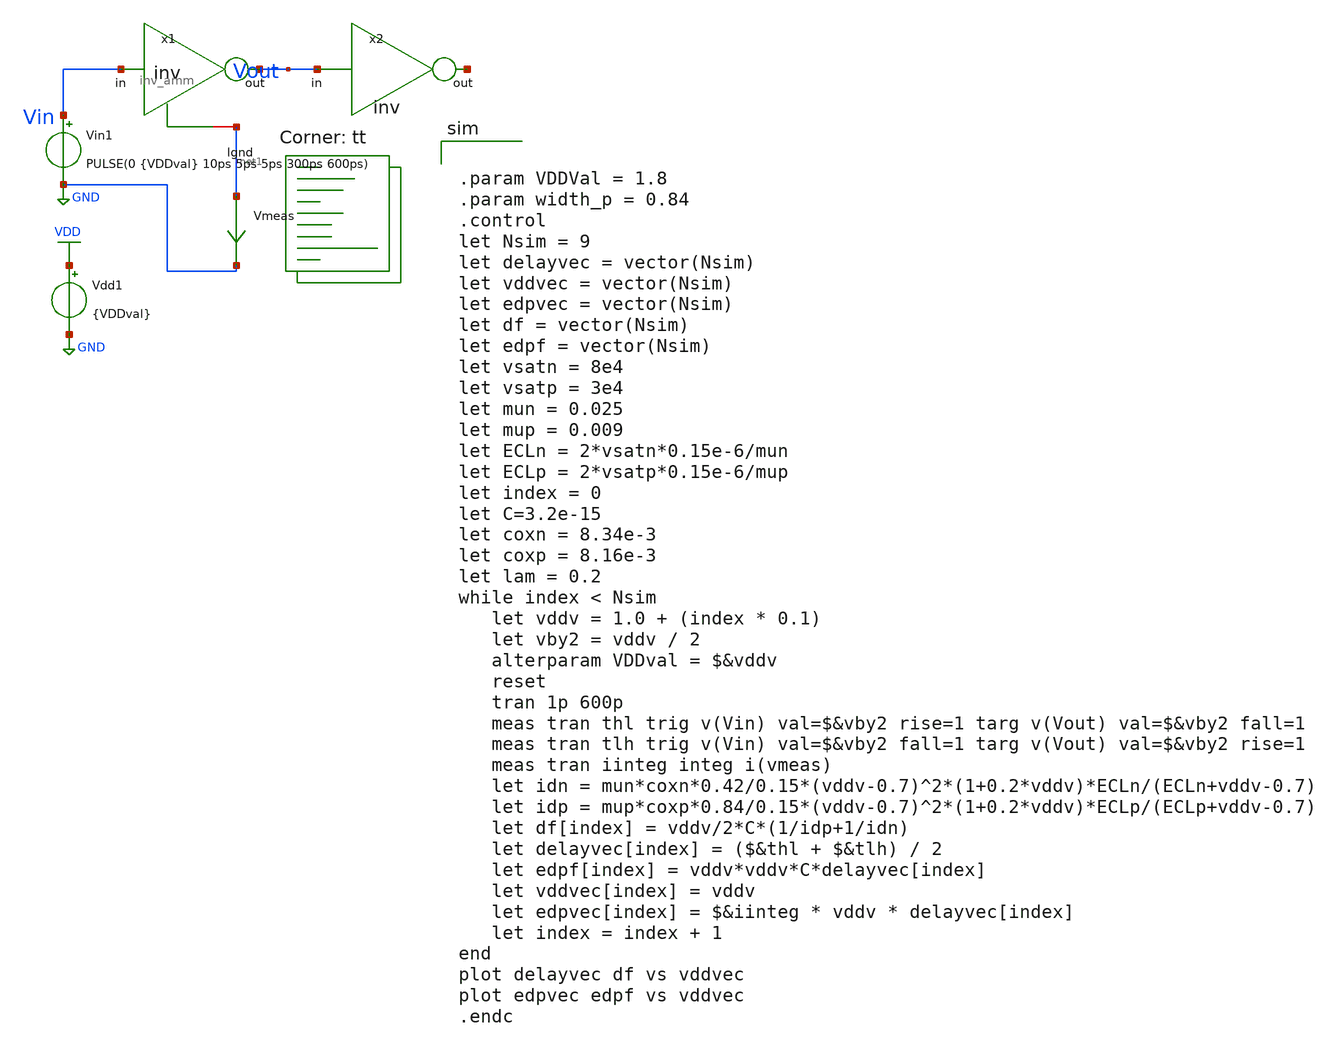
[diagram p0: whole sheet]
** sch_path: tutorial_4/tutorial_4_1c.sch
**.subckt tutorial_4_1c
x1 Vin net1 Vout inv_amm
x2 net2 Vout inv
Vin1 Vin GND PULSE(0 {VDDval} 10ps 5ps 5ps 300ps 600ps)
Vmeas net1 GND 0
Vdd1 VDD GND {VDDval}
**** begin user architecture code
.lib $::SKYWATER_MODELS/sky130.lib.spice tt


.param VDDVal = 1.8
.param width_p = 0.84
.control
let Nsim = 9
let delayvec = vector(Nsim)
let vddvec = vector(Nsim)
let edpvec = vector(Nsim)
let df = vector(Nsim)
let edpf = vector(Nsim)
let vsatn = 8e4
let vsatp = 3e4
let mun = 0.025
let mup = 0.009
let ECLn = 2*vsatn*0.15e-6/mun
let ECLp = 2*vsatp*0.15e-6/mup
let index = 0
let C=3.2e-15
let coxn = 8.34e-3
let coxp = 8.16e-3
let lam = 0.2
while index < Nsim
   let vddv = 1.0 + (index * 0.1)
   let vby2 = vddv / 2
   alterparam VDDval = $&vddv
   reset
   tran 1p 600p
   meas tran thl trig v(Vin) val=$&vby2 rise=1 targ v(Vout) val=$&vby2 fall=1
   meas tran tlh trig v(Vin) val=$&vby2 fall=1 targ v(Vout) val=$&vby2 rise=1
   meas tran iinteg integ i(vmeas)
   let idn = mun*coxn*0.42/0.15*(vddv-0.7)^2*(1+0.2*vddv)*ECLn/(ECLn+vddv-0.7)
   let idp = mup*coxp*0.84/0.15*(vddv-0.7)^2*(1+0.2*vddv)*ECLp/(ECLp+vddv-0.7)
   let df[index] = vddv/2*C*(1/idp+1/idn)
   let delayvec[index] = ($&thl + $&tlh) / 2
   let edpf[index] = vddv*vddv*C*delayvec[index]
   let vddvec[index] = vddv
   let edpvec[index] = $&iinteg * vddv * delayvec[index]
   let index = index + 1
end
plot delayvec df vs vddvec
plot edpvec edpf vs vddvec
.endc

**** end user architecture code
**.ends

* expanding   symbol:  /home/EE23B038/ee5311/tutorial_4/inv_amm.sym # of pins=3
** sym_path: tutorial_4/inv_amm.sym
** sch_path: tutorial_4/inv_amm.sch
.subckt inv_amm in lgnd out
*.ipin in
*.opin out
*.iopin lgnd
XM1 out in lgnd GND sky130_fd_pr__nfet_01v8 L=0.15 W=0.42 nf=1 ad='int((nf+1)/2) * W/nf * 0.29' as='int((nf+2)/2) * W/nf * 0.29'
+ pd='2*int((nf+1)/2) * (W/nf + 0.29)' ps='2*int((nf+2)/2) * (W/nf + 0.29)' nrd='0.29 / W' nrs='0.29 / W'
+ sa=0 sb=0 sd=0 mult=1 m=1
XM2 out in VDD VDD sky130_fd_pr__pfet_01v8 L=0.15 W={width_p} nf=1 ad='int((nf+1)/2) * W/nf * 0.29' as='int((nf+2)/2) * W/nf * 0.29'
+ pd='2*int((nf+1)/2) * (W/nf + 0.29)' ps='2*int((nf+2)/2) * (W/nf + 0.29)' nrd='0.29 / W' nrs='0.29 / W'
+ sa=0 sb=0 sd=0 mult=1 m=1
.ends


* expanding   symbol:  /home/EE23B038/ee5311/tutorial_4/inv.sym # of pins=2
** sym_path: tutorial_4/inv.sym
** sch_path: tutorial_4/inv.sch
.subckt inv out in
*.ipin in
*.opin out
XM1 out in GND GND sky130_fd_pr__nfet_01v8 L=0.15 W=0.42 nf=1 ad='int((nf+1)/2) * W/nf * 0.29' as='int((nf+2)/2) * W/nf * 0.29'
+ pd='2*int((nf+1)/2) * (W/nf + 0.29)' ps='2*int((nf+2)/2) * (W/nf + 0.29)' nrd='0.29 / W' nrs='0.29 / W'
+ sa=0 sb=0 sd=0 mult=1 m=1
XM2 out in VDD VDD sky130_fd_pr__pfet_01v8 L=0.15 W={width_p} nf=1 ad='int((nf+1)/2) * W/nf * 0.29' as='int((nf+2)/2) * W/nf * 0.29'
+ pd='2*int((nf+1)/2) * (W/nf + 0.29)' ps='2*int((nf+2)/2) * (W/nf + 0.29)' nrd='0.29 / W' nrs='0.29 / W'
+ sa=0 sb=0 sd=0 mult=1 m=1
.ends

.GLOBAL GND
.GLOBAL VDD
.end
